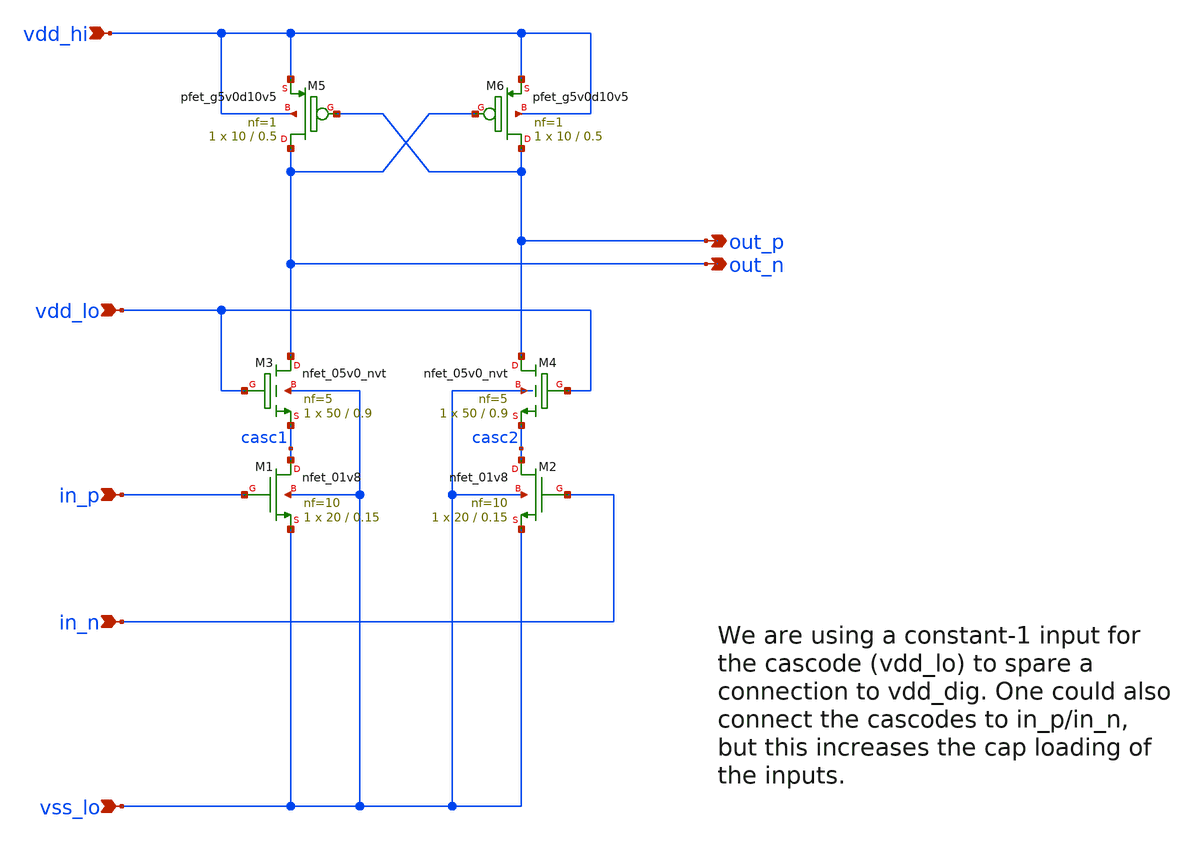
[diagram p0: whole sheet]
** sch_path: xschem/audiodac_drv_ls.sch
* (c) 2022 Harald Pretl, IIC, Johannes Kepler University
**.subckt audiodac_drv_ls in_p in_n out_p out_n vdd_hi vss_lo vdd_lo
*.ipin in_p
*.ipin in_n
*.opin out_p
*.opin out_n
*.ipin vdd_hi
*.ipin vss_lo
*.ipin vdd_lo
XM6 out_p out_n vdd_hi vdd_hi sky130_fd_pr__pfet_g5v0d10v5 L=0.5 W=10 nf=1 ad='int((1 + 1)/2) * 10 / 1 * 0.29'
+ as='int((1 + 2)/2) * 10 / 1 * 0.29' pd='2*int((1 + 1)/2) * (10 / 1 + 0.29)' ps='2*int((1 + 2)/2) * (10 / 1 + 0.29)'
+ nrd='0.29 / 10 ' nrs='0.29 / 10 ' sa=0 sb=0 sd=0 mult=1 m=1
XM5 out_n out_p vdd_hi vdd_hi sky130_fd_pr__pfet_g5v0d10v5 L=0.5 W=10 nf=1 ad='int((1 + 1)/2) * 10 / 1 * 0.29'
+ as='int((1 + 2)/2) * 10 / 1 * 0.29' pd='2*int((1 + 1)/2) * (10 / 1 + 0.29)' ps='2*int((1 + 2)/2) * (10 / 1 + 0.29)'
+ nrd='0.29 / 10 ' nrs='0.29 / 10 ' sa=0 sb=0 sd=0 mult=1 m=1
XM1 casc1 in_p vss_lo vss_lo sky130_fd_pr__nfet_01v8 L=0.15 W=20 nf=10 ad='int((10 + 1)/2) * 20 / 10 * 0.29'
+ as='int((10 + 2)/2) * 20 / 10 * 0.29' pd='2*int((10 + 1)/2) * (20 / 10 + 0.29)' ps='2*int((10 + 2)/2) * (20 / 10 + 0.29)'
+ nrd='0.29 / 20 ' nrs='0.29 / 20 ' sa=0 sb=0 sd=0 mult=1 m=1
XM2 casc2 in_n vss_lo vss_lo sky130_fd_pr__nfet_01v8 L=0.15 W=20 nf=10 ad='int((10 + 1)/2) * 20 / 10 * 0.29'
+ as='int((10 + 2)/2) * 20 / 10 * 0.29' pd='2*int((10 + 1)/2) * (20 / 10 + 0.29)' ps='2*int((10 + 2)/2) * (20 / 10 + 0.29)'
+ nrd='0.29 / 20 ' nrs='0.29 / 20 ' sa=0 sb=0 sd=0 mult=1 m=1
XM3 out_n vdd_lo casc1 vss_lo sky130_fd_pr__nfet_05v0_nvt L=0.9 W=50 nf=5 ad='int((5 + 1)/2) * 50 / 5 * 0.29'
+ as='int((5 + 2)/2) * 50 / 5 * 0.29' pd='2*int((5 + 1)/2) * (50 / 5 + 0.29)' ps='2*int((5 + 2)/2) * (50 / 5 + 0.29)'
+ nrd='0.29 / 50 ' nrs='0.29 / 50 ' sa=0 sb=0 sd=0 mult=1 m=1
XM4 out_p vdd_lo casc2 vss_lo sky130_fd_pr__nfet_05v0_nvt L=0.9 W=50 nf=5 ad='int((5 + 1)/2) * 50 / 5 * 0.29'
+ as='int((5 + 2)/2) * 50 / 5 * 0.29' pd='2*int((5 + 1)/2) * (50 / 5 + 0.29)' ps='2*int((5 + 2)/2) * (50 / 5 + 0.29)'
+ nrd='0.29 / 50 ' nrs='0.29 / 50 ' sa=0 sb=0 sd=0 mult=1 m=1
**.ends
.end
